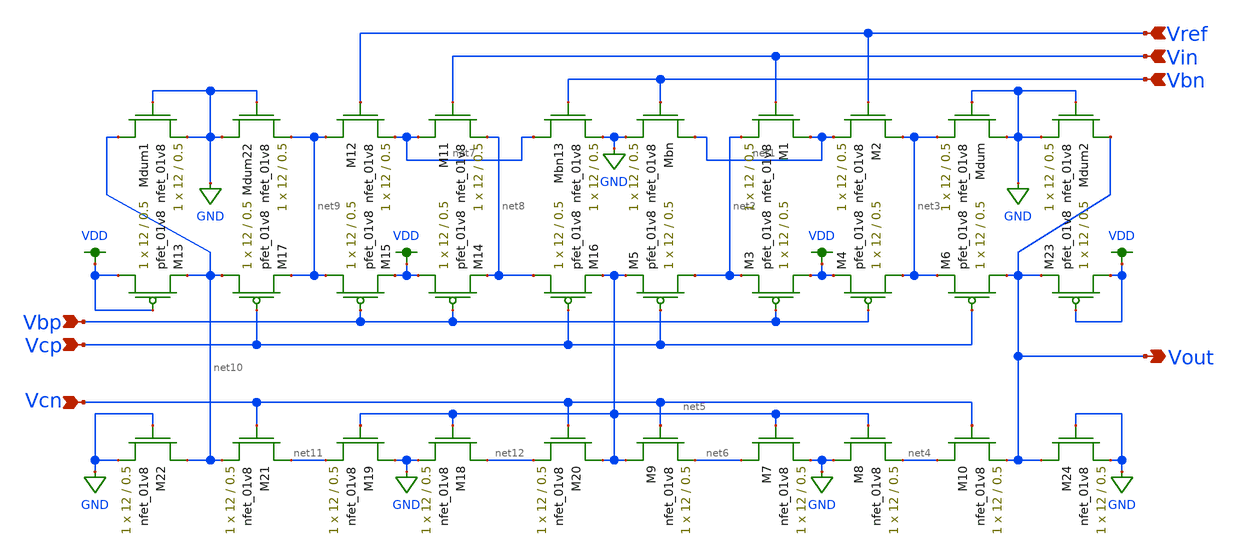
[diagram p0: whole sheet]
** sch_path: MP3/correction/xschem/diffamp_lds.sch
**.subckt diffamp_lds Vin Vref Vbn Vout Vbp Vcp Vcn
*.ipin Vin
*.ipin Vref
*.ipin Vbn
*.opin Vout
*.ipin Vbp
*.ipin Vcp
*.ipin Vcn
XM1 net1 Vin net2 GND sky130_fd_pr__nfet_01v8 L=0.5 W=12 nf=1 ad='int((nf+1)/2) * W/nf * 0.29' as='int((nf+2)/2) * W/nf * 0.29'
+ pd='2*int((nf+1)/2) * (W/nf + 0.29)' ps='2*int((nf+2)/2) * (W/nf + 0.29)' nrd='0.29 / W' nrs='0.29 / W'
+ sa=0 sb=0 sd=0 mult=1 m=1
XM2 net3 Vref net1 GND sky130_fd_pr__nfet_01v8 L=0.5 W=12 nf=1 ad='int((nf+1)/2) * W/nf * 0.29' as='int((nf+2)/2) * W/nf * 0.29'
+ pd='2*int((nf+1)/2) * (W/nf + 0.29)' ps='2*int((nf+2)/2) * (W/nf + 0.29)' nrd='0.29 / W' nrs='0.29 / W'
+ sa=0 sb=0 sd=0 mult=1 m=1
XMbn net1 Vbn GND GND sky130_fd_pr__nfet_01v8 L=0.5 W=12 nf=1 ad='int((nf+1)/2) * W/nf * 0.29' as='int((nf+2)/2) * W/nf * 0.29'
+ pd='2*int((nf+1)/2) * (W/nf + 0.29)' ps='2*int((nf+2)/2) * (W/nf + 0.29)' nrd='0.29 / W' nrs='0.29 / W'
+ sa=0 sb=0 sd=0 mult=1 m=1
XM3 VDD Vbp net2 VDD sky130_fd_pr__pfet_01v8 L=0.5 W=12 nf=1 ad='int((nf+1)/2) * W/nf * 0.29' as='int((nf+2)/2) * W/nf * 0.29'
+ pd='2*int((nf+1)/2) * (W/nf + 0.29)' ps='2*int((nf+2)/2) * (W/nf + 0.29)' nrd='0.29 / W' nrs='0.29 / W'
+ sa=0 sb=0 sd=0 mult=1 m=1
XM4 net3 Vbp VDD VDD sky130_fd_pr__pfet_01v8 L=0.5 W=12 nf=1 ad='int((nf+1)/2) * W/nf * 0.29' as='int((nf+2)/2) * W/nf * 0.29'
+ pd='2*int((nf+1)/2) * (W/nf + 0.29)' ps='2*int((nf+2)/2) * (W/nf + 0.29)' nrd='0.29 / W' nrs='0.29 / W'
+ sa=0 sb=0 sd=0 mult=1 m=1
XM5 net2 Vcp net5 VDD sky130_fd_pr__pfet_01v8 L=0.5 W=12 nf=1 ad='int((nf+1)/2) * W/nf * 0.29' as='int((nf+2)/2) * W/nf * 0.29'
+ pd='2*int((nf+1)/2) * (W/nf + 0.29)' ps='2*int((nf+2)/2) * (W/nf + 0.29)' nrd='0.29 / W' nrs='0.29 / W'
+ sa=0 sb=0 sd=0 mult=1 m=1
XM6 Vout Vcp net3 VDD sky130_fd_pr__pfet_01v8 L=0.5 W=12 nf=1 ad='int((nf+1)/2) * W/nf * 0.29' as='int((nf+2)/2) * W/nf * 0.29'
+ pd='2*int((nf+1)/2) * (W/nf + 0.29)' ps='2*int((nf+2)/2) * (W/nf + 0.29)' nrd='0.29 / W' nrs='0.29 / W'
+ sa=0 sb=0 sd=0 mult=1 m=1
XM7 net6 net5 GND GND sky130_fd_pr__nfet_01v8 L=0.5 W=12 nf=1 ad='int((nf+1)/2) * W/nf * 0.29' as='int((nf+2)/2) * W/nf * 0.29'
+ pd='2*int((nf+1)/2) * (W/nf + 0.29)' ps='2*int((nf+2)/2) * (W/nf + 0.29)' nrd='0.29 / W' nrs='0.29 / W'
+ sa=0 sb=0 sd=0 mult=1 m=1
XM8 GND net5 net4 GND sky130_fd_pr__nfet_01v8 L=0.5 W=12 nf=1 ad='int((nf+1)/2) * W/nf * 0.29' as='int((nf+2)/2) * W/nf * 0.29'
+ pd='2*int((nf+1)/2) * (W/nf + 0.29)' ps='2*int((nf+2)/2) * (W/nf + 0.29)' nrd='0.29 / W' nrs='0.29 / W'
+ sa=0 sb=0 sd=0 mult=1 m=1
XM9 net5 Vcn net6 GND sky130_fd_pr__nfet_01v8 L=0.5 W=12 nf=1 ad='int((nf+1)/2) * W/nf * 0.29' as='int((nf+2)/2) * W/nf * 0.29'
+ pd='2*int((nf+1)/2) * (W/nf + 0.29)' ps='2*int((nf+2)/2) * (W/nf + 0.29)' nrd='0.29 / W' nrs='0.29 / W'
+ sa=0 sb=0 sd=0 mult=1 m=1
XM10 net4 Vcn Vout GND sky130_fd_pr__nfet_01v8 L=0.5 W=12 nf=1 ad='int((nf+1)/2) * W/nf * 0.29' as='int((nf+2)/2) * W/nf * 0.29'
+ pd='2*int((nf+1)/2) * (W/nf + 0.29)' ps='2*int((nf+2)/2) * (W/nf + 0.29)' nrd='0.29 / W' nrs='0.29 / W'
+ sa=0 sb=0 sd=0 mult=1 m=1
XMdum GND GND net3 GND sky130_fd_pr__nfet_01v8 L=0.5 W=12 nf=1 ad='int((nf+1)/2) * W/nf * 0.29' as='int((nf+2)/2) * W/nf * 0.29'
+ pd='2*int((nf+1)/2) * (W/nf + 0.29)' ps='2*int((nf+2)/2) * (W/nf + 0.29)' nrd='0.29 / W' nrs='0.29 / W'
+ sa=0 sb=0 sd=0 mult=1 m=1
XM11 net7 Vin net8 GND sky130_fd_pr__nfet_01v8 L=0.5 W=12 nf=1 ad='int((nf+1)/2) * W/nf * 0.29' as='int((nf+2)/2) * W/nf * 0.29'
+ pd='2*int((nf+1)/2) * (W/nf + 0.29)' ps='2*int((nf+2)/2) * (W/nf + 0.29)' nrd='0.29 / W' nrs='0.29 / W'
+ sa=0 sb=0 sd=0 mult=1 m=1
XM12 net9 Vref net7 GND sky130_fd_pr__nfet_01v8 L=0.5 W=12 nf=1 ad='int((nf+1)/2) * W/nf * 0.29' as='int((nf+2)/2) * W/nf * 0.29'
+ pd='2*int((nf+1)/2) * (W/nf + 0.29)' ps='2*int((nf+2)/2) * (W/nf + 0.29)' nrd='0.29 / W' nrs='0.29 / W'
+ sa=0 sb=0 sd=0 mult=1 m=1
XMbn13 net7 Vbn GND GND sky130_fd_pr__nfet_01v8 L=0.5 W=12 nf=1 ad='int((nf+1)/2) * W/nf * 0.29' as='int((nf+2)/2) * W/nf * 0.29'
+ pd='2*int((nf+1)/2) * (W/nf + 0.29)' ps='2*int((nf+2)/2) * (W/nf + 0.29)' nrd='0.29 / W' nrs='0.29 / W'
+ sa=0 sb=0 sd=0 mult=1 m=1
XM14 VDD Vbp net8 VDD sky130_fd_pr__pfet_01v8 L=0.5 W=12 nf=1 ad='int((nf+1)/2) * W/nf * 0.29' as='int((nf+2)/2) * W/nf * 0.29'
+ pd='2*int((nf+1)/2) * (W/nf + 0.29)' ps='2*int((nf+2)/2) * (W/nf + 0.29)' nrd='0.29 / W' nrs='0.29 / W'
+ sa=0 sb=0 sd=0 mult=1 m=1
XM15 net9 Vbp VDD VDD sky130_fd_pr__pfet_01v8 L=0.5 W=12 nf=1 ad='int((nf+1)/2) * W/nf * 0.29' as='int((nf+2)/2) * W/nf * 0.29'
+ pd='2*int((nf+1)/2) * (W/nf + 0.29)' ps='2*int((nf+2)/2) * (W/nf + 0.29)' nrd='0.29 / W' nrs='0.29 / W'
+ sa=0 sb=0 sd=0 mult=1 m=1
XM16 net8 Vcp net5 VDD sky130_fd_pr__pfet_01v8 L=0.5 W=12 nf=1 ad='int((nf+1)/2) * W/nf * 0.29' as='int((nf+2)/2) * W/nf * 0.29'
+ pd='2*int((nf+1)/2) * (W/nf + 0.29)' ps='2*int((nf+2)/2) * (W/nf + 0.29)' nrd='0.29 / W' nrs='0.29 / W'
+ sa=0 sb=0 sd=0 mult=1 m=1
XM17 net10 Vcp net9 VDD sky130_fd_pr__pfet_01v8 L=0.5 W=12 nf=1 ad='int((nf+1)/2) * W/nf * 0.29' as='int((nf+2)/2) * W/nf * 0.29'
+ pd='2*int((nf+1)/2) * (W/nf + 0.29)' ps='2*int((nf+2)/2) * (W/nf + 0.29)' nrd='0.29 / W' nrs='0.29 / W'
+ sa=0 sb=0 sd=0 mult=1 m=1
XM18 net12 net5 GND GND sky130_fd_pr__nfet_01v8 L=0.5 W=12 nf=1 ad='int((nf+1)/2) * W/nf * 0.29' as='int((nf+2)/2) * W/nf * 0.29'
+ pd='2*int((nf+1)/2) * (W/nf + 0.29)' ps='2*int((nf+2)/2) * (W/nf + 0.29)' nrd='0.29 / W' nrs='0.29 / W'
+ sa=0 sb=0 sd=0 mult=1 m=1
XM19 GND net5 net11 GND sky130_fd_pr__nfet_01v8 L=0.5 W=12 nf=1 ad='int((nf+1)/2) * W/nf * 0.29' as='int((nf+2)/2) * W/nf * 0.29'
+ pd='2*int((nf+1)/2) * (W/nf + 0.29)' ps='2*int((nf+2)/2) * (W/nf + 0.29)' nrd='0.29 / W' nrs='0.29 / W'
+ sa=0 sb=0 sd=0 mult=1 m=1
XM20 net5 Vcn net12 GND sky130_fd_pr__nfet_01v8 L=0.5 W=12 nf=1 ad='int((nf+1)/2) * W/nf * 0.29' as='int((nf+2)/2) * W/nf * 0.29'
+ pd='2*int((nf+1)/2) * (W/nf + 0.29)' ps='2*int((nf+2)/2) * (W/nf + 0.29)' nrd='0.29 / W' nrs='0.29 / W'
+ sa=0 sb=0 sd=0 mult=1 m=1
XM21 net11 Vcn net10 GND sky130_fd_pr__nfet_01v8 L=0.5 W=12 nf=1 ad='int((nf+1)/2) * W/nf * 0.29' as='int((nf+2)/2) * W/nf * 0.29'
+ pd='2*int((nf+1)/2) * (W/nf + 0.29)' ps='2*int((nf+2)/2) * (W/nf + 0.29)' nrd='0.29 / W' nrs='0.29 / W'
+ sa=0 sb=0 sd=0 mult=1 m=1
XMdum22 GND GND net9 GND sky130_fd_pr__nfet_01v8 L=0.5 W=12 nf=1 ad='int((nf+1)/2) * W/nf * 0.29' as='int((nf+2)/2) * W/nf * 0.29'
+ pd='2*int((nf+1)/2) * (W/nf + 0.29)' ps='2*int((nf+2)/2) * (W/nf + 0.29)' nrd='0.29 / W' nrs='0.29 / W'
+ sa=0 sb=0 sd=0 mult=1 m=1
XMdum1 net10 GND GND GND sky130_fd_pr__nfet_01v8 L=0.5 W=12 nf=1 ad='int((nf+1)/2) * W/nf * 0.29' as='int((nf+2)/2) * W/nf * 0.29'
+ pd='2*int((nf+1)/2) * (W/nf + 0.29)' ps='2*int((nf+2)/2) * (W/nf + 0.29)' nrd='0.29 / W' nrs='0.29 / W'
+ sa=0 sb=0 sd=0 mult=1 m=1
XM13 VDD VDD net10 VDD sky130_fd_pr__pfet_01v8 L=0.5 W=12 nf=1 ad='int((nf+1)/2) * W/nf * 0.29' as='int((nf+2)/2) * W/nf * 0.29'
+ pd='2*int((nf+1)/2) * (W/nf + 0.29)' ps='2*int((nf+2)/2) * (W/nf + 0.29)' nrd='0.29 / W' nrs='0.29 / W'
+ sa=0 sb=0 sd=0 mult=1 m=1
XM22 net10 GND GND GND sky130_fd_pr__nfet_01v8 L=0.5 W=12 nf=1 ad='int((nf+1)/2) * W/nf * 0.29' as='int((nf+2)/2) * W/nf * 0.29'
+ pd='2*int((nf+1)/2) * (W/nf + 0.29)' ps='2*int((nf+2)/2) * (W/nf + 0.29)' nrd='0.29 / W' nrs='0.29 / W'
+ sa=0 sb=0 sd=0 mult=1 m=1
XMdum2 Vout GND GND GND sky130_fd_pr__nfet_01v8 L=0.5 W=12 nf=1 ad='int((nf+1)/2) * W/nf * 0.29' as='int((nf+2)/2) * W/nf * 0.29'
+ pd='2*int((nf+1)/2) * (W/nf + 0.29)' ps='2*int((nf+2)/2) * (W/nf + 0.29)' nrd='0.29 / W' nrs='0.29 / W'
+ sa=0 sb=0 sd=0 mult=1 m=1
XM23 VDD VDD Vout VDD sky130_fd_pr__pfet_01v8 L=0.5 W=12 nf=1 ad='int((nf+1)/2) * W/nf * 0.29' as='int((nf+2)/2) * W/nf * 0.29'
+ pd='2*int((nf+1)/2) * (W/nf + 0.29)' ps='2*int((nf+2)/2) * (W/nf + 0.29)' nrd='0.29 / W' nrs='0.29 / W'
+ sa=0 sb=0 sd=0 mult=1 m=1
XM24 Vout GND GND GND sky130_fd_pr__nfet_01v8 L=0.5 W=12 nf=1 ad='int((nf+1)/2) * W/nf * 0.29' as='int((nf+2)/2) * W/nf * 0.29'
+ pd='2*int((nf+1)/2) * (W/nf + 0.29)' ps='2*int((nf+2)/2) * (W/nf + 0.29)' nrd='0.29 / W' nrs='0.29 / W'
+ sa=0 sb=0 sd=0 mult=1 m=1
**.ends
.GLOBAL GND
.GLOBAL VDD
.end
